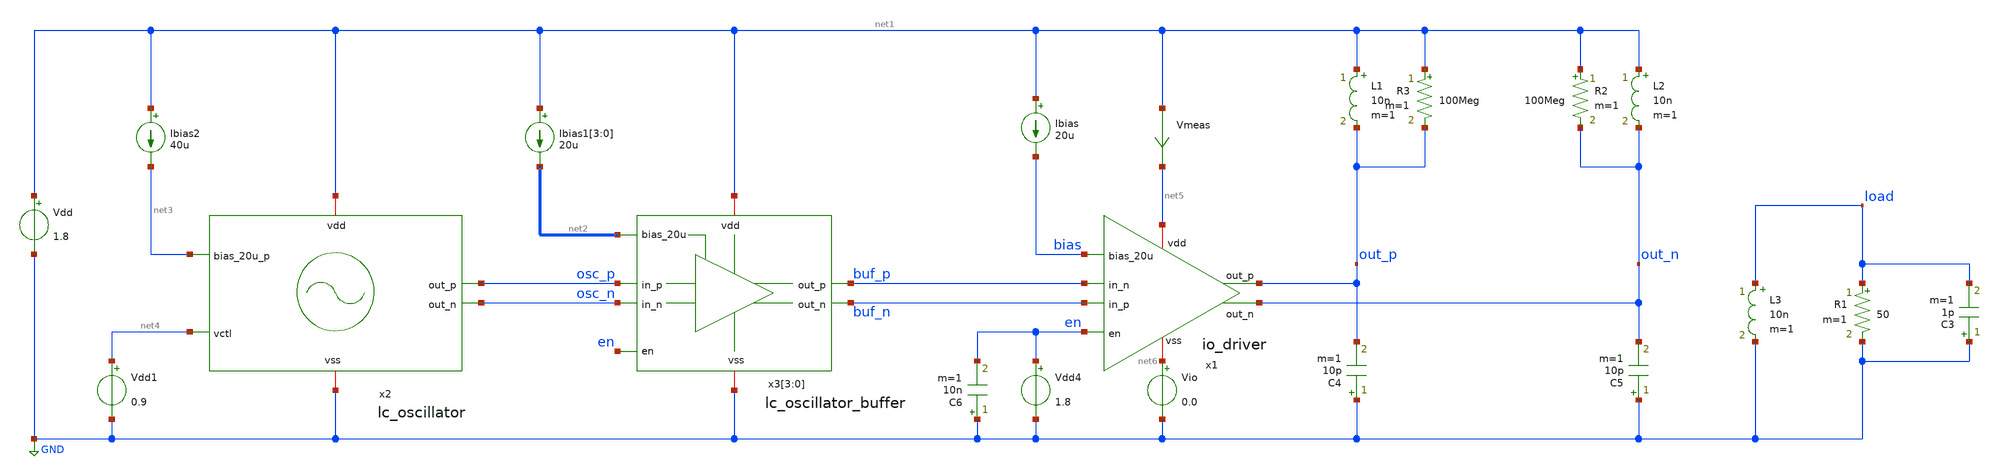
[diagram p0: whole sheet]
** sch_path: design/io_driver/test/io_buffer_test.sch
**.subckt io_buffer_test
L1 net1 out_p 10n m=1
L2 net1 out_n 10n m=1
L3 load GND 10n m=1
R1 load GND 50 m=1
Vdd net1 GND 1.8
Ibias net1 bias 20u
C3 GND load 1p m=1
R2 net1 out_n 100Meg m=1
R3 net1 out_p 100Meg m=1
x1 net5 en bias out_p out_n buf_p buf_n net6 io_driver
Vdd4 en GND 1.8
C4 GND out_p 10p m=1
C5 GND out_n 10p m=1
x2 net1 osc_p net4 osc_n net3 GND lc_oscillator
x3[3] net1 osc_p osc_n buf_p buf_n GND net2[3] en lc_oscillator_buffer
x3[2] net1 osc_p osc_n buf_p buf_n GND net2[2] en lc_oscillator_buffer
x3[1] net1 osc_p osc_n buf_p buf_n GND net2[1] en lc_oscillator_buffer
x3[0] net1 osc_p osc_n buf_p buf_n GND net2[0] en lc_oscillator_buffer
Ibias1[3] net1 net2[3] 20u
Ibias1[2] net1 net2[2] 20u
Ibias1[1] net1 net2[1] 20u
Ibias1[0] net1 net2[0] 20u
Ibias2 net1 net3 40u
Vdd1 net4 GND 0.9
C6 GND en 10n m=1
Vio net6 GND 0.0
Vmeas net1 net5 0
.save i(vmeas)
**** begin user architecture code


.param temp=27

*.op
.tran 1p 100n
*.ac dec 100 100 100G

*.options rshunt=1e11

K1 L1 L3 0.7
K2 L2 L3 -0.7

.save all





.options wnflag=1
.include $::SKYWATER_MODELS/cells/nfet_01v8/sky130_fd_pr__nfet_01v8__tt.corner.spice
.include $::SKYWATER_MODELS/cells/nfet_01v8_lvt/sky130_fd_pr__nfet_01v8_lvt__tt.corner.spice
.include $::SKYWATER_MODELS/cells/pfet_01v8/sky130_fd_pr__pfet_01v8__tt.corner.spice
.include $::SKYWATER_MODELS/cells/nfet_03v3_nvt/sky130_fd_pr__nfet_03v3_nvt__tt.corner.spice
.include $::SKYWATER_MODELS/cells/nfet_05v0_nvt/sky130_fd_pr__nfet_05v0_nvt__tt.corner.spice
.include $::SKYWATER_MODELS/cells/esd_nfet_01v8/sky130_fd_pr__esd_nfet_01v8__tt.corner.spice
.include $::SKYWATER_MODELS/cells/pfet_01v8_lvt/sky130_fd_pr__pfet_01v8_lvt__tt.corner.spice
.include $::SKYWATER_MODELS/cells/pfet_01v8_hvt/sky130_fd_pr__pfet_01v8_hvt__tt.corner.spice
.include $::SKYWATER_MODELS/cells/esd_pfet_g5v0d10v5/sky130_fd_pr__esd_pfet_g5v0d10v5__tt.corner.spice
.include $::SKYWATER_MODELS/cells/pfet_g5v0d10v5/sky130_fd_pr__pfet_g5v0d10v5__tt.corner.spice
.include $::SKYWATER_MODELS/cells/pfet_g5v0d16v0/sky130_fd_pr__pfet_g5v0d16v0__tt.corner.spice
.include $::SKYWATER_MODELS/cells/nfet_g5v0d10v5/sky130_fd_pr__nfet_g5v0d10v5__tt.corner.spice
.include $::SKYWATER_MODELS/cells/nfet_g5v0d16v0/sky130_fd_pr__nfet_g5v0d16v0__tt_discrete.corner.spice
.include $::SKYWATER_MODELS/cells/esd_nfet_g5v0d10v5/sky130_fd_pr__esd_nfet_g5v0d10v5__tt.corner.spice
.include $::SKYWATER_MODELS/models/corners/tt/nonfet.spice
* Mismatch parameters
.include $::SKYWATER_MODELS/cells/nfet_01v8/sky130_fd_pr__nfet_01v8__mismatch.corner.spice
.include $::SKYWATER_MODELS/cells/pfet_01v8/sky130_fd_pr__pfet_01v8__mismatch.corner.spice
.include $::SKYWATER_MODELS/cells/nfet_01v8_lvt/sky130_fd_pr__nfet_01v8_lvt__mismatch.corner.spice
.include $::SKYWATER_MODELS/cells/pfet_01v8_lvt/sky130_fd_pr__pfet_01v8_lvt__mismatch.corner.spice
.include $::SKYWATER_MODELS/cells/pfet_01v8_hvt/sky130_fd_pr__pfet_01v8_hvt__mismatch.corner.spice
.include $::SKYWATER_MODELS/cells/nfet_g5v0d10v5/sky130_fd_pr__nfet_g5v0d10v5__mismatch.corner.spice
.include $::SKYWATER_MODELS/cells/pfet_g5v0d10v5/sky130_fd_pr__pfet_g5v0d10v5__mismatch.corner.spice
.include $::SKYWATER_MODELS/cells/nfet_05v0_nvt/sky130_fd_pr__nfet_05v0_nvt__mismatch.corner.spice
.include $::SKYWATER_MODELS/cells/nfet_03v3_nvt/sky130_fd_pr__nfet_03v3_nvt__mismatch.corner.spice
* Resistor$::SKYWATER_MODELS/Capacitor
.include $::SKYWATER_MODELS/models/r+c/res_typical__cap_typical.spice
.include $::SKYWATER_MODELS/models/r+c/res_typical__cap_typical__lin.spice
* Special cells
.include $::SKYWATER_MODELS/models/corners/tt/specialized_cells.spice
* All models
.include $::SKYWATER_MODELS/models/all.spice
* Corner
.include $::SKYWATER_MODELS/models/corners/tt/rf.spice

 [sky130_models]
**** end user architecture code
**.ends
.GLOBAL GND
.end
